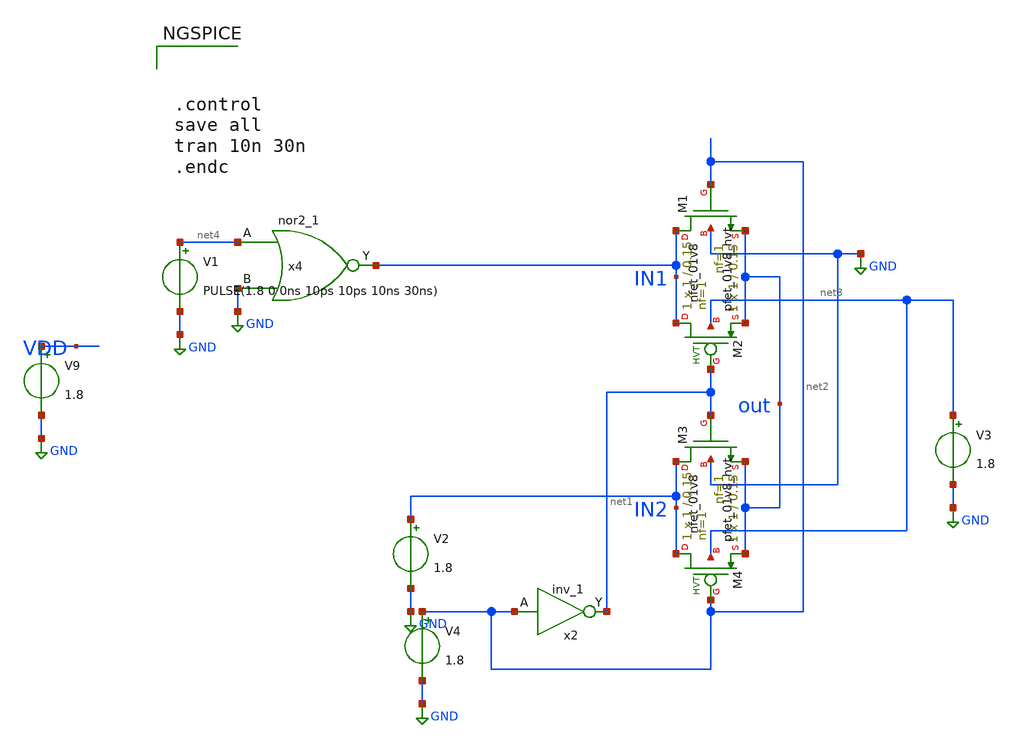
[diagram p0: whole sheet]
** sch_path: xiaolin/nor_tb.sch
**.subckt nor_tb
XM1 IN1 net2 out GND sky130_fd_pr__nfet_01v8 L=0.15 W=1 nf=1 ad='int((nf+1)/2) * W/nf * 0.29' as='int((nf+2)/2) * W/nf * 0.29'
+ pd='2*int((nf+1)/2) * (W/nf + 0.29)' ps='2*int((nf+2)/2) * (W/nf + 0.29)' nrd='0.29 / W' nrs='0.29 / W'
+ sa=0 sb=0 sd=0 mult=1 m=1
XM2 IN1 net1 out net3 sky130_fd_pr__pfet_01v8_hvt L=0.15 W=1 nf=1 ad='int((nf+1)/2) * W/nf * 0.29' as='int((nf+2)/2) * W/nf * 0.29'
+ pd='2*int((nf+1)/2) * (W/nf + 0.29)' ps='2*int((nf+2)/2) * (W/nf + 0.29)' nrd='0.29 / W' nrs='0.29 / W'
+ sa=0 sb=0 sd=0 mult=1 m=1
XM3 IN2 net1 out GND sky130_fd_pr__nfet_01v8 L=0.15 W=1 nf=1 ad='int((nf+1)/2) * W/nf * 0.29' as='int((nf+2)/2) * W/nf * 0.29'
+ pd='2*int((nf+1)/2) * (W/nf + 0.29)' ps='2*int((nf+2)/2) * (W/nf + 0.29)' nrd='0.29 / W' nrs='0.29 / W'
+ sa=0 sb=0 sd=0 mult=1 m=1
XM4 IN2 net2 out net3 sky130_fd_pr__pfet_01v8_hvt L=0.15 W=1 nf=1 ad='int((nf+1)/2) * W/nf * 0.29' as='int((nf+2)/2) * W/nf * 0.29'
+ pd='2*int((nf+1)/2) * (W/nf + 0.29)' ps='2*int((nf+2)/2) * (W/nf + 0.29)' nrd='0.29 / W' nrs='0.29 / W'
+ sa=0 sb=0 sd=0 mult=1 m=1
V3 net3 GND 1.8
x2 net2 GND GND VDD VDD net1 sky130_fd_sc_hd__inv_1
V4 net2 GND 1.8
V9 VDD GND 1.8
V2 IN2 GND 1.8
x4 net4 GND GND GND VDD VDD IN1 sky130_fd_sc_hd__nor2_1
V1 net4 GND PULSE(1.8 0 0ns 10ps 10ps 10ns 30ns)
**** begin user architecture code


.lib /farmshare/home/classes/ee/372/PDKs/open_pdks/sky130/sky130A/libs.tech/ngspice/sky130.lib.spice tt
.include /farmshare/home/classes/ee/372/PDKs/open_pdks/sky130/sky130A/libs.ref/sky130_fd_sc_hd/spice/sky130_fd_sc_hd.spice






.control
save all
tran 10n 30n
.endc


**** end user architecture code
**.ends
.GLOBAL GND
.end
